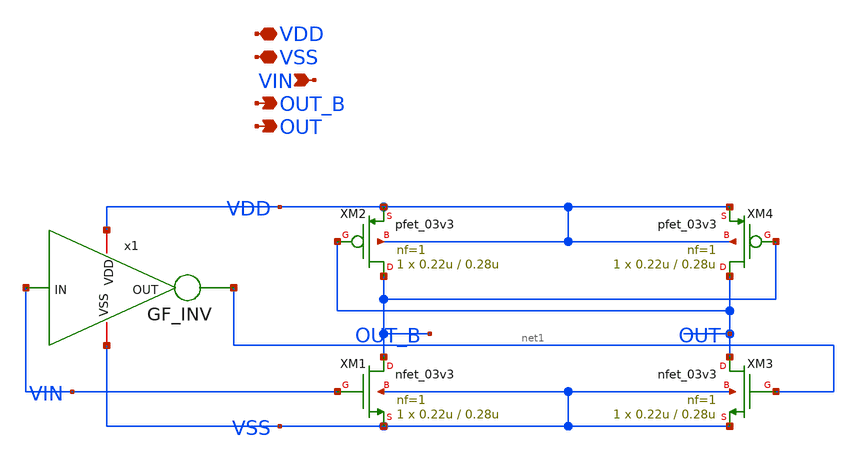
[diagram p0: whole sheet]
** sch_path: DAC_PAKISTAN_01/Pakistan1_Xschem/Balanced_Inverter.sch
**.subckt Balanced_Inverter VSS VIN OUT_B VDD OUT
*.iopin VSS
*.ipin VIN
*.opin OUT_B
*.iopin VDD
*.opin OUT
XM1 OUT_B VIN VSS VSS nfet_03v3 L=0.28u W=0.22u nf=1 ad='int((nf+1)/2) * W/nf * 0.18u' as='int((nf+2)/2) * W/nf * 0.18u'
+ pd='2*int((nf+1)/2) * (W/nf + 0.18u)' ps='2*int((nf+2)/2) * (W/nf + 0.18u)' nrd='0.18u / W' nrs='0.18u / W'
+ sa=0 sb=0 sd=0 m=1
XM2 OUT_B OUT VDD VDD pfet_03v3 L=0.28u W=0.22u nf=1 ad='int((nf+1)/2) * W/nf * 0.18u' as='int((nf+2)/2) * W/nf * 0.18u'
+ pd='2*int((nf+1)/2) * (W/nf + 0.18u)' ps='2*int((nf+2)/2) * (W/nf + 0.18u)' nrd='0.18u / W' nrs='0.18u / W'
+ sa=0 sb=0 sd=0 m=1
XM3 OUT net1 VSS VSS nfet_03v3 L=0.28u W=0.22u nf=1 ad='int((nf+1)/2) * W/nf * 0.18u' as='int((nf+2)/2) * W/nf * 0.18u'
+ pd='2*int((nf+1)/2) * (W/nf + 0.18u)' ps='2*int((nf+2)/2) * (W/nf + 0.18u)' nrd='0.18u / W' nrs='0.18u / W'
+ sa=0 sb=0 sd=0 m=1
XM4 OUT OUT_B VDD VDD pfet_03v3 L=0.28u W=0.22u nf=1 ad='int((nf+1)/2) * W/nf * 0.18u' as='int((nf+2)/2) * W/nf * 0.18u'
+ pd='2*int((nf+1)/2) * (W/nf + 0.18u)' ps='2*int((nf+2)/2) * (W/nf + 0.18u)' nrd='0.18u / W' nrs='0.18u / W'
+ sa=0 sb=0 sd=0 m=1
x1 VSS VDD net1 VIN GF_INV
**.ends

* expanding   symbol:  GF_INV.sym # of pins=4
** sym_path: GF_INV.sym
** sch_path: GF_INV.sch
.subckt GF_INV VSS VDD OUT IN
*.iopin VDD
*.iopin VSS
*.ipin IN
*.opin OUT
XM1 OUT IN VSS VSS nfet_03v3 L=0.28u W=0.25u nf=1 ad='int((nf+1)/2) * W/nf * 0.18u' as='int((nf+2)/2) * W/nf * 0.18u'
+ pd='2*int((nf+1)/2) * (W/nf + 0.18u)' ps='2*int((nf+2)/2) * (W/nf + 0.18u)' nrd='0.18u / W' nrs='0.18u / W'
+ sa=0 sb=0 sd=0 m=1
XM2 OUT IN VDD VDD pfet_03v3 L=0.28u W=0.5u nf=1 ad='int((nf+1)/2) * W/nf * 0.18u' as='int((nf+2)/2) * W/nf * 0.18u'
+ pd='2*int((nf+1)/2) * (W/nf + 0.18u)' ps='2*int((nf+2)/2) * (W/nf + 0.18u)' nrd='0.18u / W' nrs='0.18u / W'
+ sa=0 sb=0 sd=0 m=1
.ends

.end
